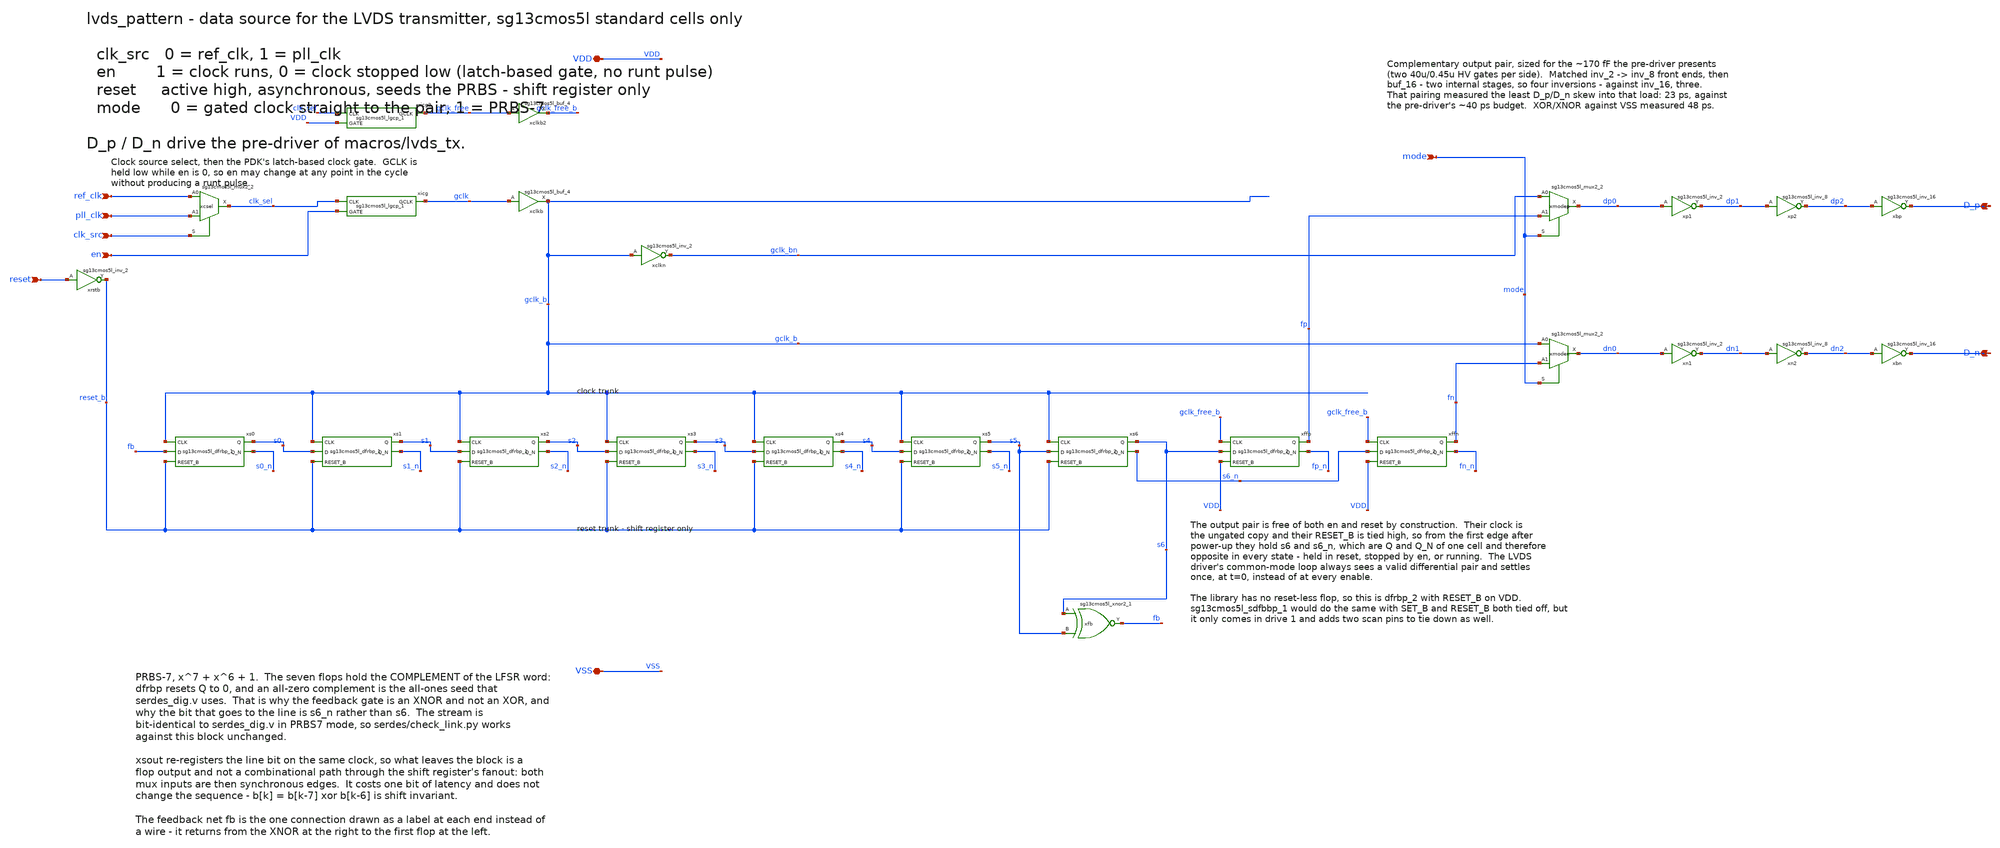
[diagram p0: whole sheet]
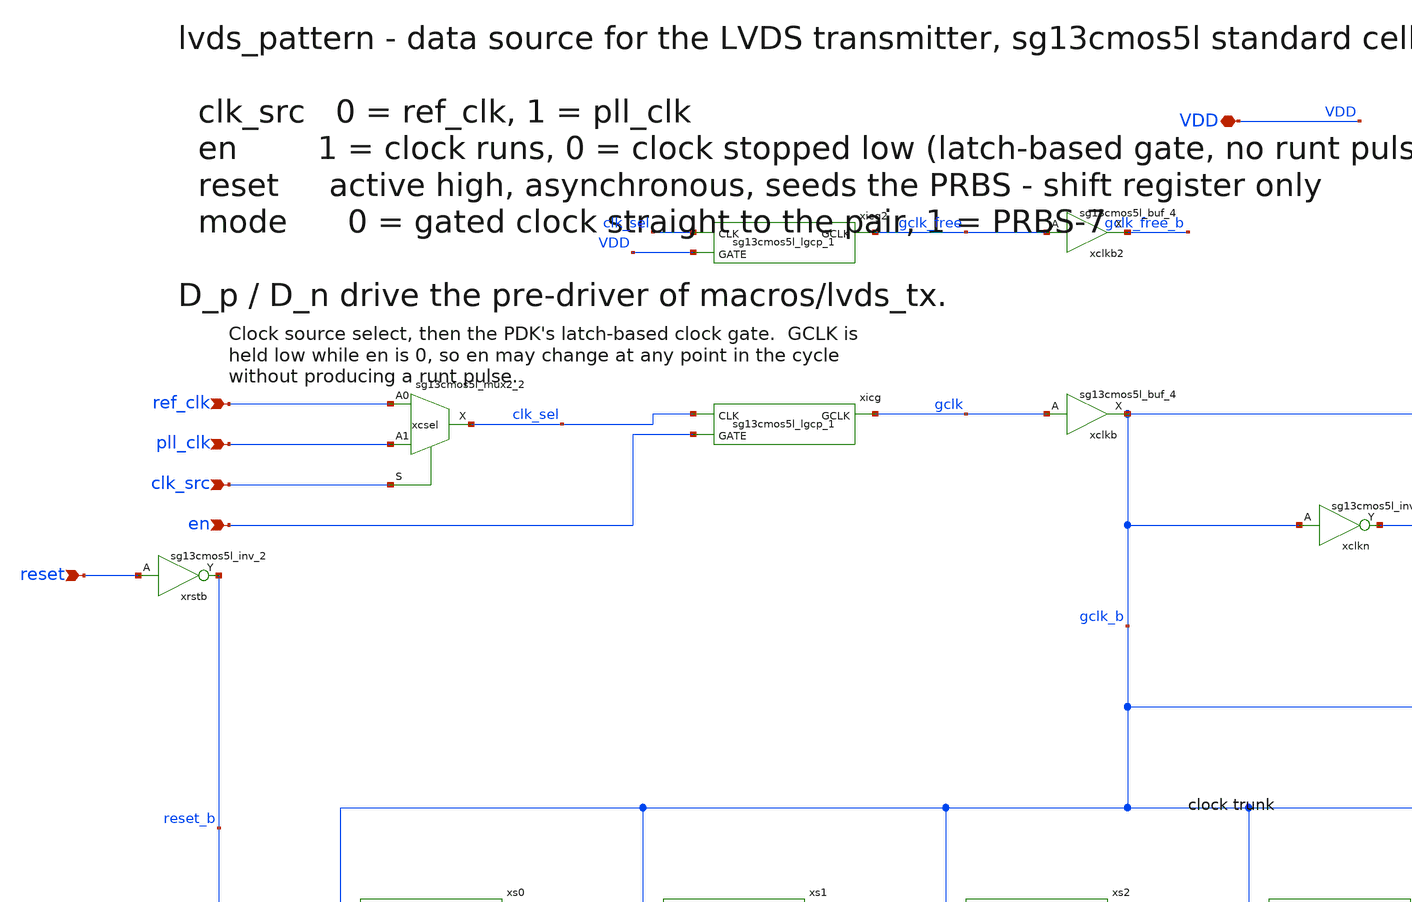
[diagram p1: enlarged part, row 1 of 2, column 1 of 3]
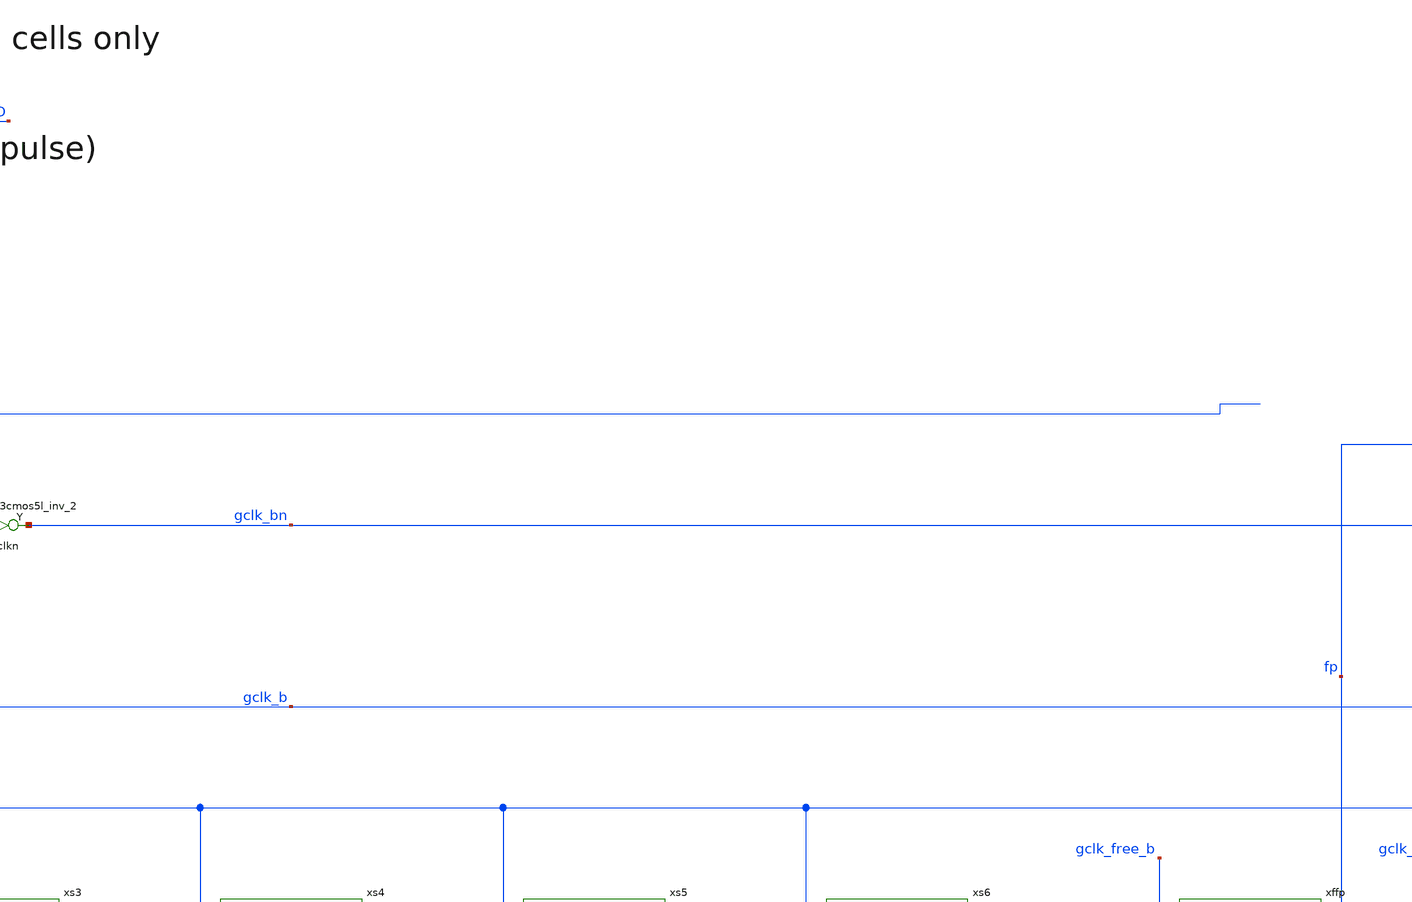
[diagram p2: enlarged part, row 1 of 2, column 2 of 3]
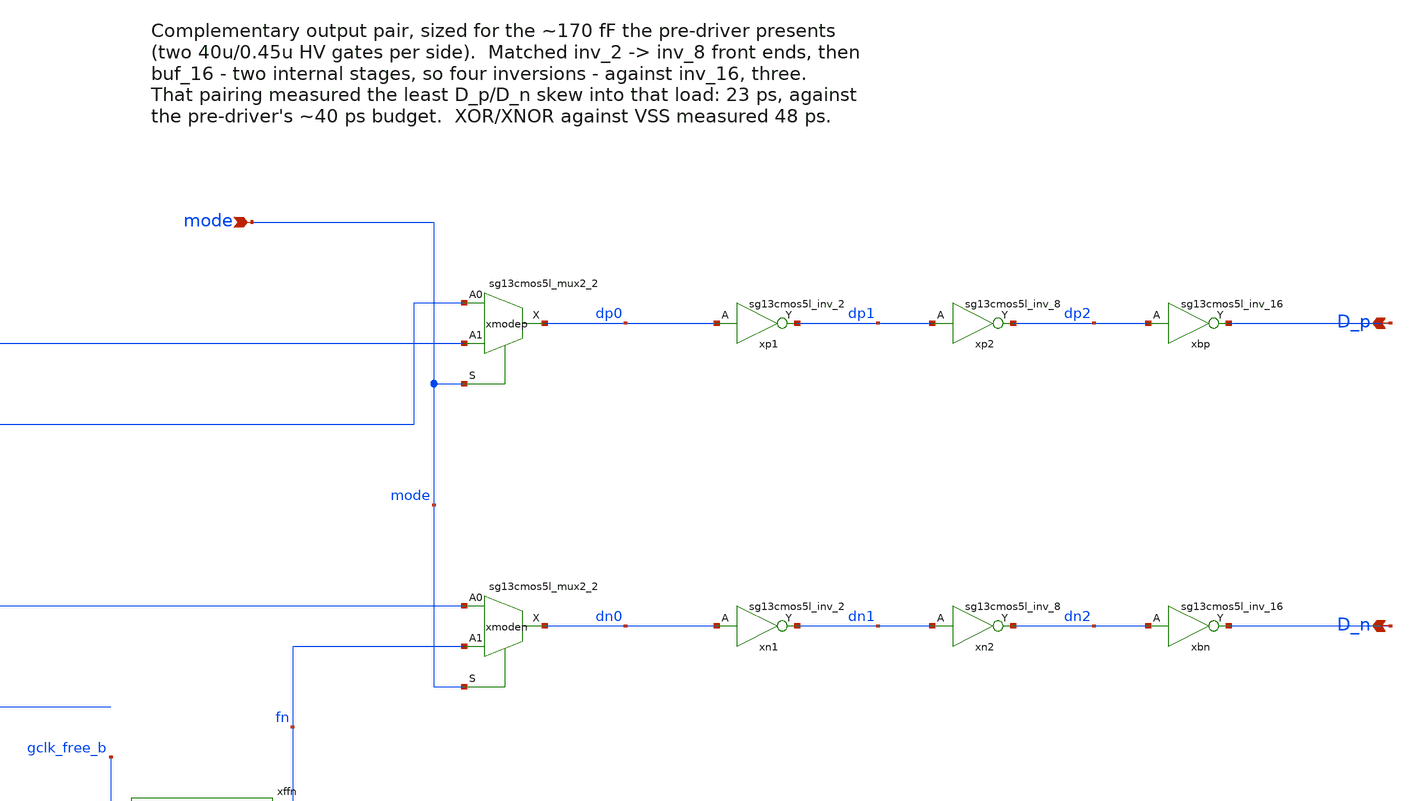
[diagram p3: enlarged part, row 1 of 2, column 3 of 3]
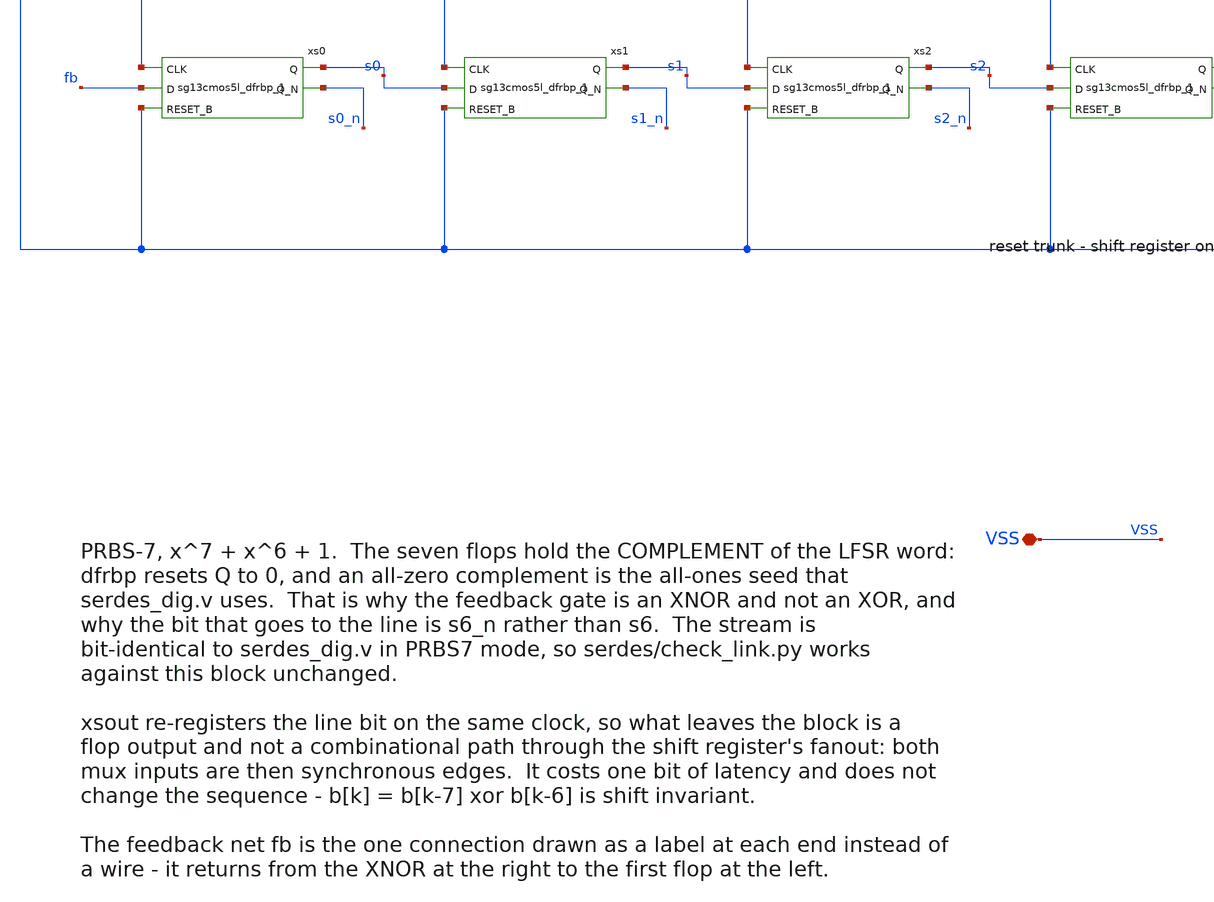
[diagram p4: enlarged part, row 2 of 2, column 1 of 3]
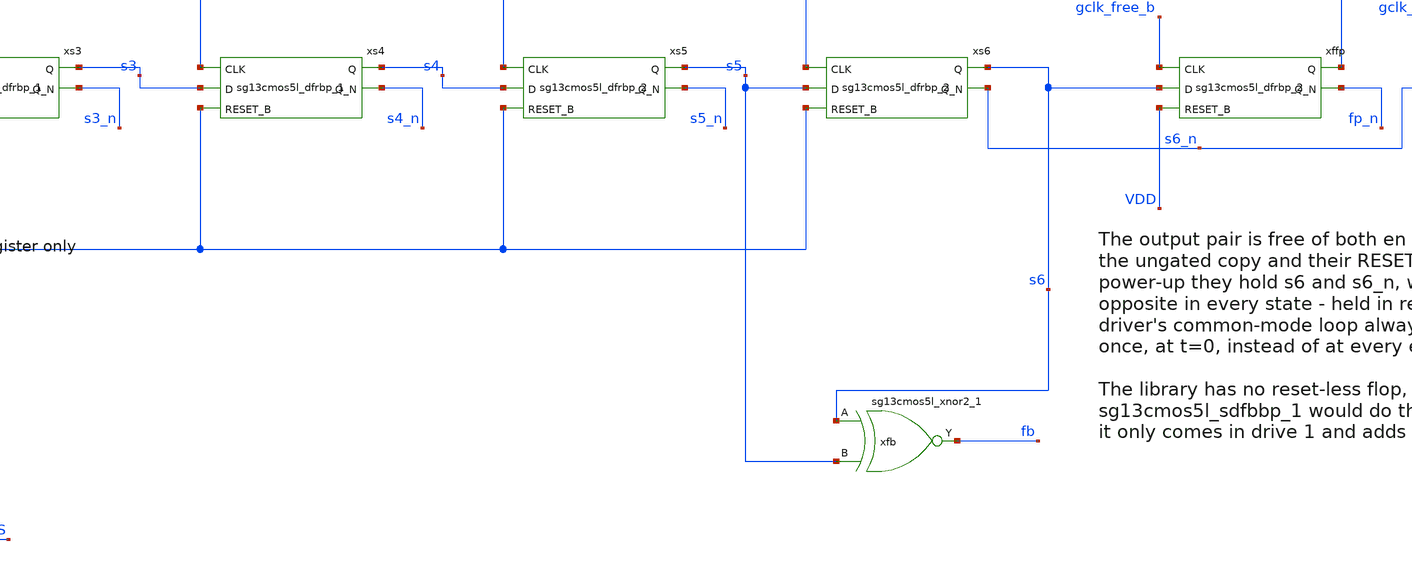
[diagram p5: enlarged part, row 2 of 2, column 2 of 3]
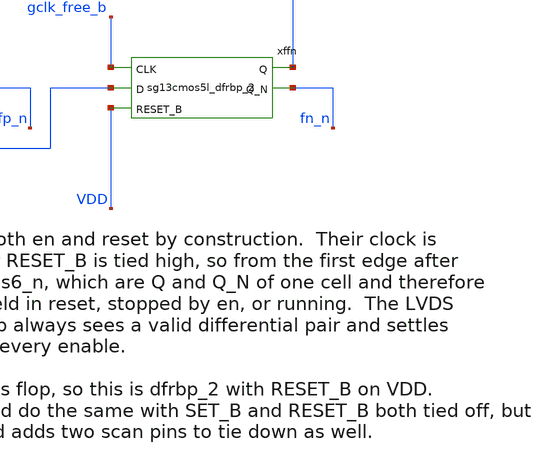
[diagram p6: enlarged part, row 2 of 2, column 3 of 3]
** sch_path: macros/lvds_pattern/schematic/xschem/lvds_pattern.sch
**.subckt lvds_pattern ref_clk pll_clk clk_src en reset mode D_p D_n VDD VSS
*.ipin ref_clk
*.ipin pll_clk
*.ipin clk_src
*.ipin en
*.ipin reset
*.ipin mode
*.opin D_p
*.opin D_n
*.iopin VDD
*.iopin VSS
xcsel clk_sel ref_clk pll_clk clk_src VDD VSS sg13cmos5l_mux2_2
xicg gclk clk_sel en VDD VSS sg13cmos5l_lgcp_1
xclkb gclk_b gclk VDD VSS sg13cmos5l_buf_4
xicg2 gclk_free clk_sel VDD VDD VSS sg13cmos5l_lgcp_1
xclkb2 gclk_free_b gclk_free VDD VSS sg13cmos5l_buf_4
xrstb reset_b reset VDD VSS sg13cmos5l_inv_2
xs0 s0 s0_n gclk_b fb reset_b VDD VSS sg13cmos5l_dfrbp_1
xs1 s1 s1_n gclk_b s0 reset_b VDD VSS sg13cmos5l_dfrbp_1
xs2 s2 s2_n gclk_b s1 reset_b VDD VSS sg13cmos5l_dfrbp_1
xs3 s3 s3_n gclk_b s2 reset_b VDD VSS sg13cmos5l_dfrbp_1
xs4 s4 s4_n gclk_b s3 reset_b VDD VSS sg13cmos5l_dfrbp_1
xs5 s5 s5_n gclk_b s4 reset_b VDD VSS sg13cmos5l_dfrbp_2
xs6 s6 s6_n gclk_b s5 reset_b VDD VSS sg13cmos5l_dfrbp_2
xfb fb s6 s5 VDD VSS sg13cmos5l_xnor2_1
xffp fp fp_n gclk_free_b s6 VDD VDD VSS sg13cmos5l_dfrbp_2
xffn fn fn_n gclk_free_b s6_n VDD VDD VSS sg13cmos5l_dfrbp_2
xclkn gclk_bn gclk_b VDD VSS sg13cmos5l_inv_2
xmodep dp0 gclk_bn fp mode VDD VSS sg13cmos5l_mux2_2
xmoden dn0 gclk_b fn mode VDD VSS sg13cmos5l_mux2_2
xp1 dp1 dp0 VDD VSS sg13cmos5l_inv_2
xp2 dp2 dp1 VDD VSS sg13cmos5l_inv_8
xbp D_p dp2 VDD VSS sg13cmos5l_inv_16
xn1 dn1 dn0 VDD VSS sg13cmos5l_inv_2
xn2 dn2 dn1 VDD VSS sg13cmos5l_inv_8
xbn D_n dn2 VDD VSS sg13cmos5l_inv_16
**.ends
.end
